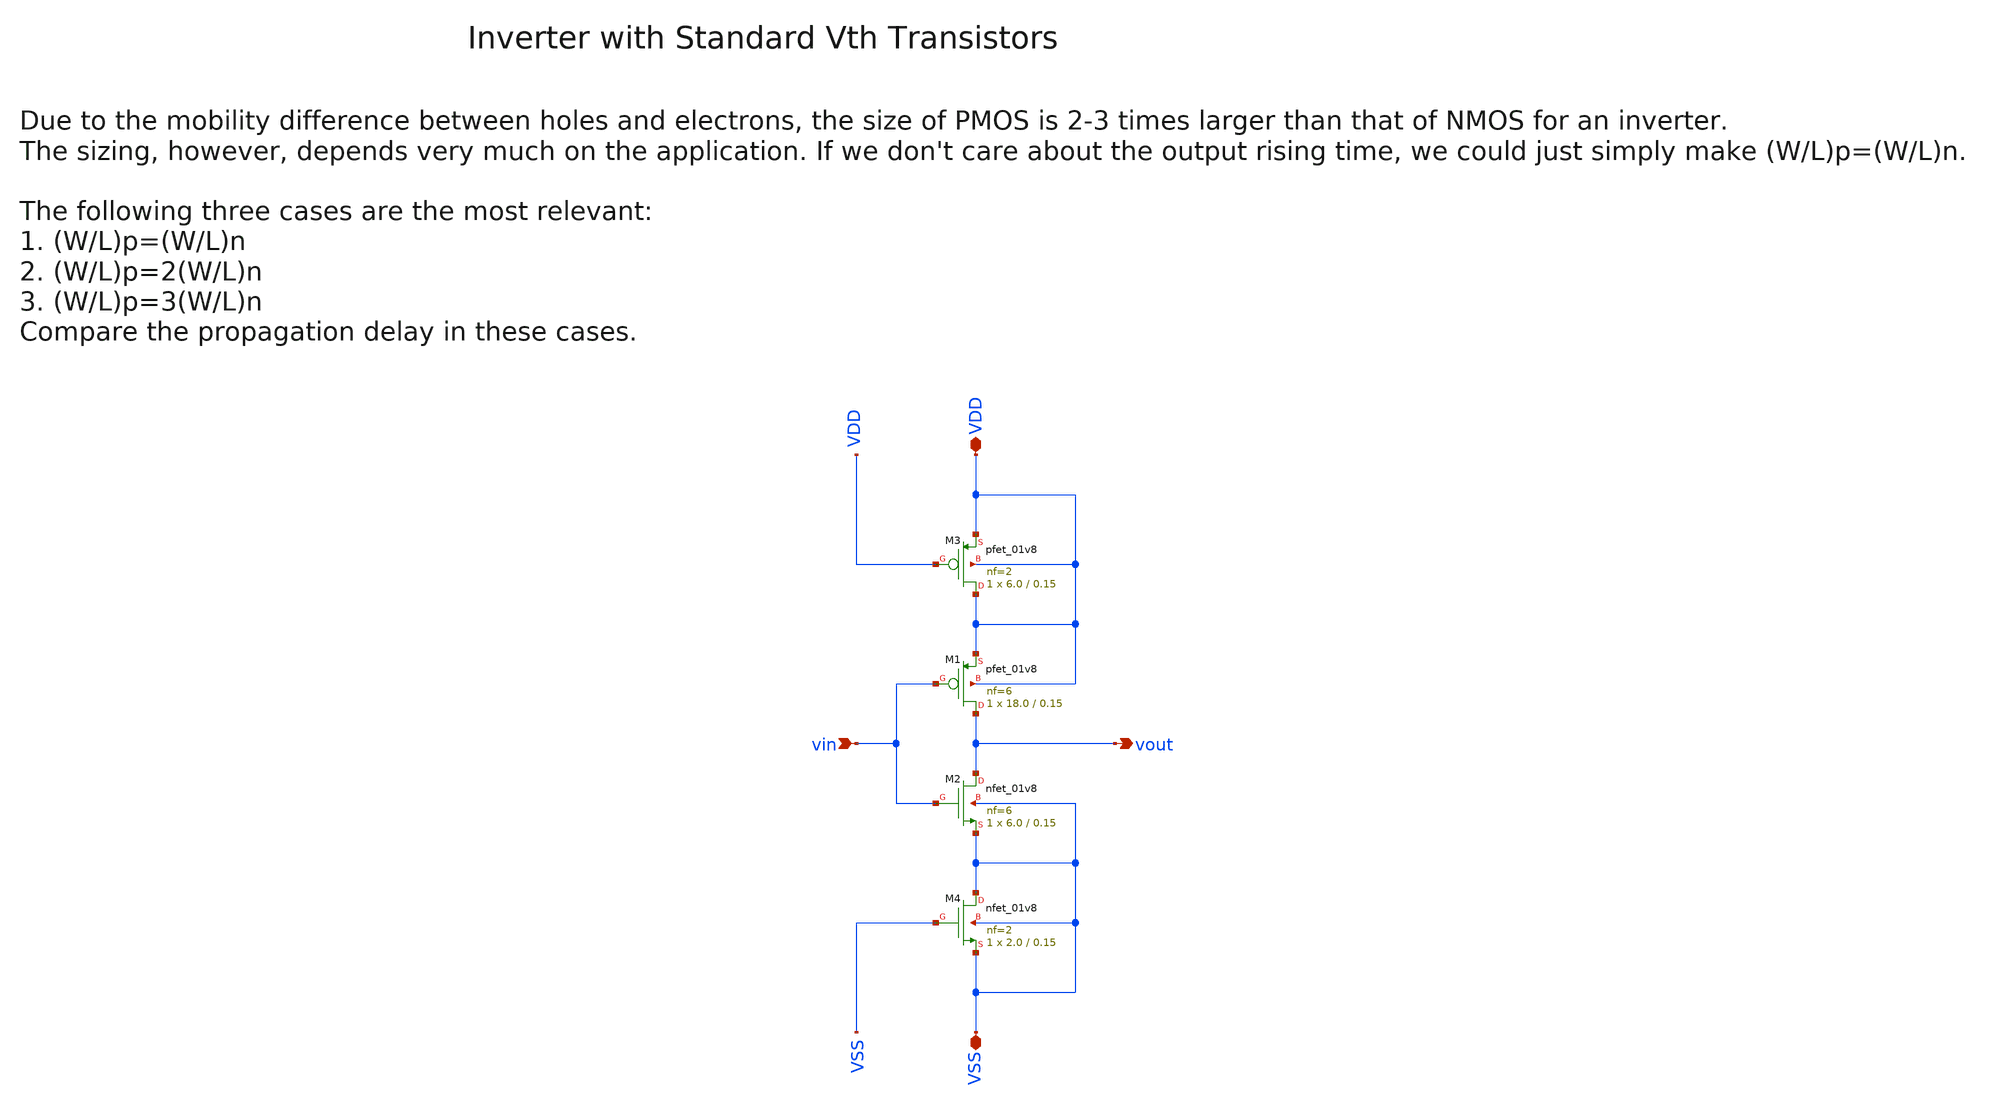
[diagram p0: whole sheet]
** sch_path: sky130/xschem/wspr_tx_iqmod_mixer_lo_logic_inv_NF6.sch
**.subckt wspr_tx_iqmod_mixer_lo_logic_inv_NF6 vin VDD VSS vout
*.ipin vin
*.iopin VDD
*.iopin VSS
*.opin vout
XM1 vout vin VDD VDD sky130_fd_pr__pfet_01v8 L=0.15 W=18.0 nf=6 ad='int((6 + 1)/2) * 18.0 / 6 * 0.29'
+ as='int((6 + 2)/2) * 18.0 / 6 * 0.29' pd='2*int((6 + 1)/2) * (18.0 / 6 + 0.29)' ps='2*int((6 + 2)/2) * (18.0 / 6 + 0.29)'
+ nrd='0.29 / 18.0 ' nrs='0.29 / 18.0 ' sa=0 sb=0 sd=0 mult=1 m=1
XM3 VDD VDD VDD VDD sky130_fd_pr__pfet_01v8 L=0.15 W=6.0 nf=2 ad='int((2 + 1)/2) * 6.0 / 2 * 0.29' as='int((2 + 2)/2) * 6.0 / 2 * 0.29'
+ pd='2*int((2 + 1)/2) * (6.0 / 2 + 0.29)' ps='2*int((2 + 2)/2) * (6.0 / 2 + 0.29)' nrd='0.29 / 6.0 ' nrs='0.29 / 6.0 '
+ sa=0 sb=0 sd=0 mult=1 m=1
XM2 vout vin VSS VSS sky130_fd_pr__nfet_01v8 L=0.15 W=6.0 nf=6 ad='int((6 + 1)/2) * 6.0 / 6 * 0.29' as='int((6 + 2)/2) * 6.0 / 6 * 0.29'
+ pd='2*int((6 + 1)/2) * (6.0 / 6 + 0.29)' ps='2*int((6 + 2)/2) * (6.0 / 6 + 0.29)' nrd='0.29 / 6.0 ' nrs='0.29 / 6.0 '
+ sa=0 sb=0 sd=0 mult=1 m=1
XM4 VSS VSS VSS VSS sky130_fd_pr__nfet_01v8 L=0.15 W=2.0 nf=2 ad='int((2 + 1)/2) * 2.0 / 2 * 0.29' as='int((2 + 2)/2) * 2.0 / 2 * 0.29'
+ pd='2*int((2 + 1)/2) * (2.0 / 2 + 0.29)' ps='2*int((2 + 2)/2) * (2.0 / 2 + 0.29)' nrd='0.29 / 2.0 ' nrs='0.29 / 2.0 '
+ sa=0 sb=0 sd=0 mult=1 m=1
**.ends
.end
